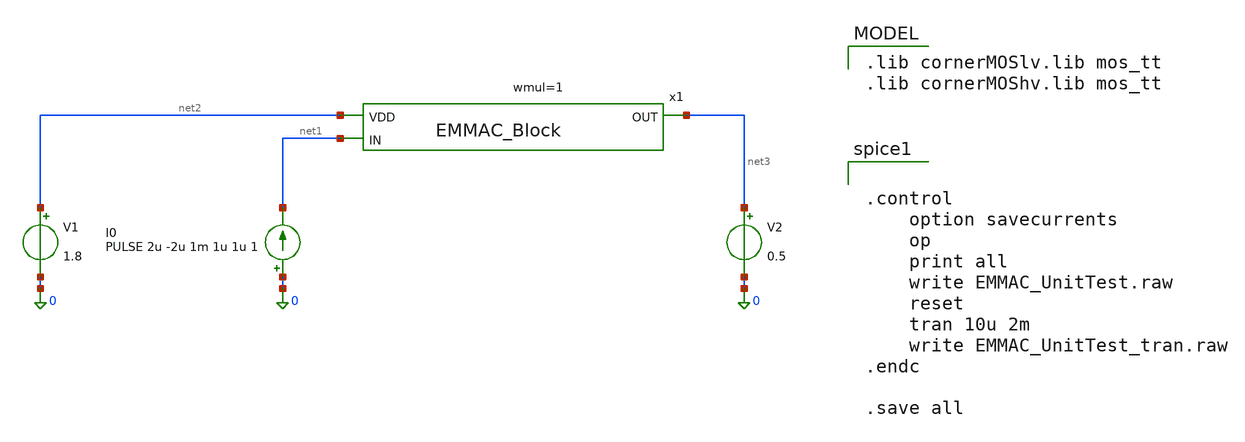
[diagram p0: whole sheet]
** sch_path: src/EMMAC_UnitTest.sch
**.subckt EMMAC_UnitTest
x1 net2 net1 net3 EMMAC_Block wmul=1
V1 net2 0 1.8
I0 0 net1 PULSE 2u -2u 1m 1u 1u 1
V2 net3 0 0.5
**** begin user architecture code
 .lib cornerMOSlv.lib mos_tt
.lib cornerMOShv.lib mos_tt



.control
	option savecurrents
	op
	print all
	write EMMAC_UnitTest.raw
	reset
	tran 10u 2m
	write EMMAC_UnitTest_tran.raw
.endc

.save all


**** end user architecture code
**.ends

* expanding   symbol:  EMMAC_Block.sym # of pins=3
** sym_path: src/analog_mac/EMMAC_Block.sym
** sch_path: src/analog_mac/EMMAC_Block.sch
.subckt EMMAC_Block VDD IN OUT  wmul=1
*.opin OUT
*.ipin IN
*.ipin VDD
XM1 net5 net3 0 0 sg13_lv_nmos w=1u l=1u ng=1 m=1 mm_ok=1
XM2 net3 net3 0 0 sg13_lv_nmos w=1u l=1u ng=1 m=1 mm_ok=1
XM21 net1 net1 VDD VDD sg13_lv_pmos w=1u l=1u ng=1 m=1 mm_ok=1
XM22 net7 net1 VDD VDD sg13_lv_pmos w=1u l=1u ng=1 m=1 mm_ok=1
XM6 net2 net2 net5 0 sg13_lv_nmos w=1u l=1u ng=1 m=1 mm_ok=1
XM7 net4 net2 net3 0 sg13_lv_nmos w=1u l=1u ng=1 m=1 mm_ok=1
XM3 net8 net6 0 0 sg13_lv_nmos w=1u l=1u ng=1 m=1 mm_ok=1
XM4 net6 net6 0 0 sg13_lv_nmos w=1u l=1u ng=1 m=1 mm_ok=1
XM8 net7 net7 net8 0 sg13_lv_nmos w=1u l=1u ng=1 m=1 mm_ok=1
XM9 net4 net7 net6 0 sg13_lv_nmos w=1u l=1u ng=1 m=1 mm_ok=1
XM23 net4 net4 VDD VDD sg13_lv_pmos w=1u l=0.28u ng=1 m=1 mm_ok=1
XM24 net9 net4 VDD VDD sg13_lv_pmos w=1u l=0.28u ng=1 m={wmul} mm_ok=1
XM19 net1 net1 IN 0 sg13_hv_nmos w=0.3u l=0.45u ng=1 m=1 mm_ok=1
XM14 IN IN net2 0 sg13_hv_nmos w=0.3u l=0.45u ng=1 m=1 mm_ok=1
XM20 OUT net4 net13 VDD sg13_lv_pmos w=1u l=0.28u ng=1 m=1 mm_ok=1
XM10 net12 net10 0 0 sg13_lv_nmos w=1u l=1u ng=1 m=1 mm_ok=1
XM11 net10 net10 net11 net11 sg13_lv_nmos w=1u l=1u ng=1 m=1 mm_ok=1
XM12 net9 net9 net12 0 sg13_lv_nmos w=1u l=1u ng=1 m=1 mm_ok=1
XM13 OUT net9 net10 net11 sg13_lv_nmos w=1u l=1u ng=1 m=1 mm_ok=1
XM5 net11 net14 0 0 sg13_lv_nmos w=1u l=1u ng=1 m=1 mm_ok=1
XM25 net13 net14 VDD VDD sg13_lv_pmos w=1u l=0.28u ng=1 m=1 mm_ok=1
XM15 net14 IN 0 0 sg13_lv_nmos w=1u l=1u ng=1 m=1 mm_ok=1
XM17 net14 IN VDD VDD sg13_lv_pmos w=1u l=1u ng=1 m=1 mm_ok=1
XM16 net15 net14 0 0 sg13_lv_nmos w=1u l=1u ng=1 m=1 mm_ok=1
XM18 net15 net14 VDD VDD sg13_lv_pmos w=1u l=1u ng=1 m=1 mm_ok=1
.ends

.end
